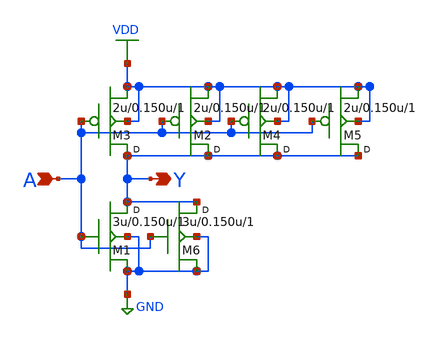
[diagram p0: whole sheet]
** sch_path: lib/xschem/schematics/INVX2.sch
**.subckt INVX2 A Y
*.ipin A
*.opin Y
M3 Y A VDD VDD pmos w=2u l=0.150u m=1
M2 Y A VDD VDD pmos w=2u l=0.150u m=1
M1 Y A GND GND nmos w=3u l=0.150u m=1
M4 Y A VDD VDD pmos w=2u l=0.150u m=1
M5 Y A VDD VDD pmos w=2u l=0.150u m=1
M6 Y A GND GND nmos w=3u l=0.150u m=1
**.ends
.GLOBAL GND
.GLOBAL VDD
.end
